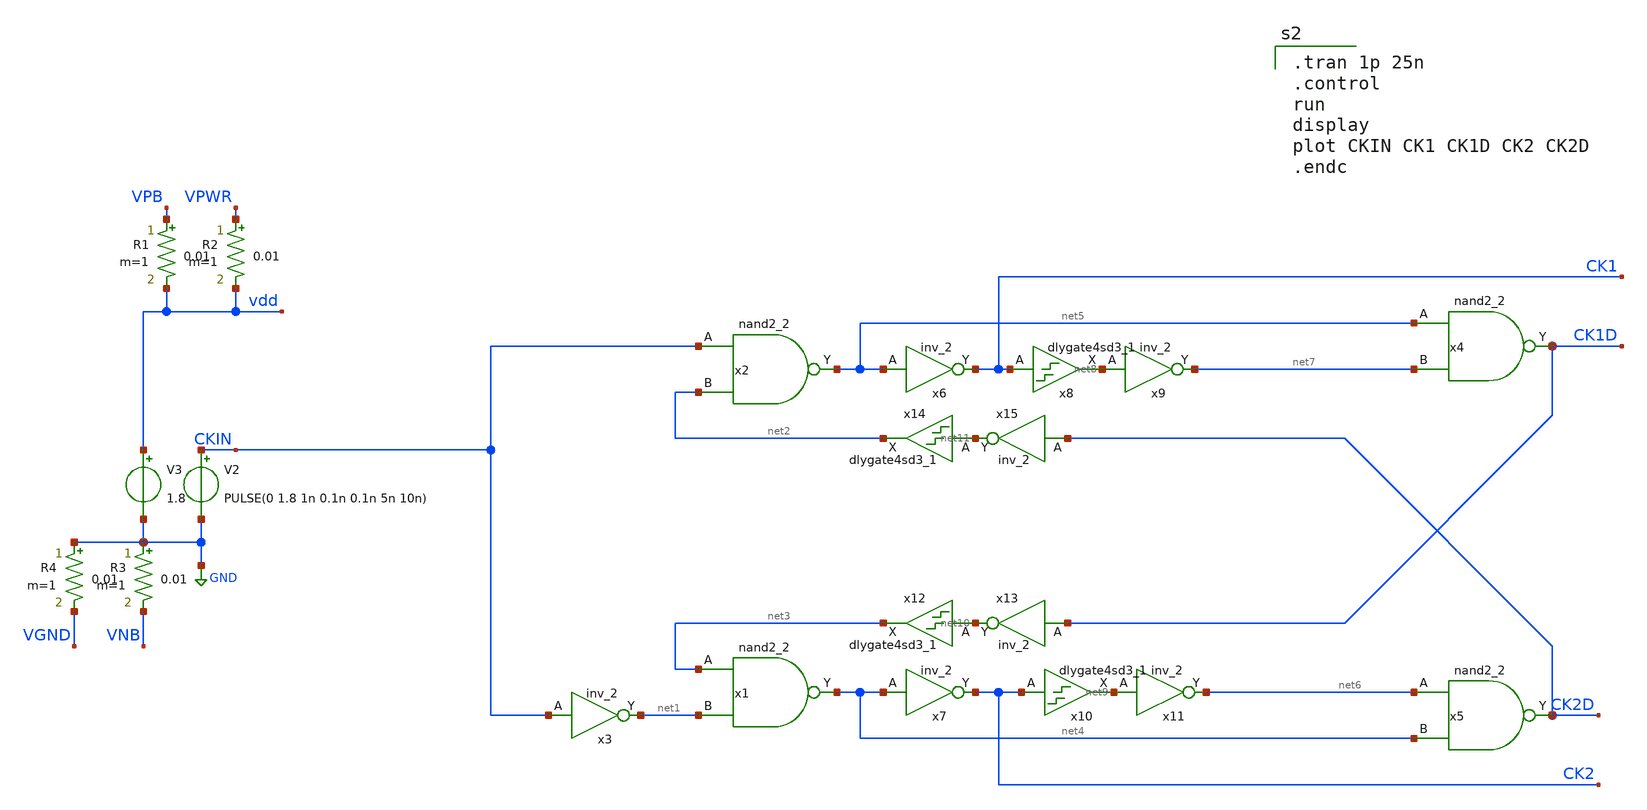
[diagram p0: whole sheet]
** sch_path: xschem/adc_non_overlap.sch
**.subckt adc_non_overlap
V2 CKIN GND PULSE(0 1.8 1n 0.1n 0.1n 5n 10n)
V3 vdd GND 1.8
x2 CKIN net2 VGND VNB VPB VPWR net5 sky130_fd_sc_hd__nand2_2
x1 net3 net1 VGND VNB VPB VPWR net4 sky130_fd_sc_hd__nand2_2
x3 CKIN VGND VNB VPB VPWR net1 sky130_fd_sc_hd__inv_2
x4 net5 net7 VGND VNB VPB VPWR CK1D sky130_fd_sc_hd__nand2_2
x5 net6 net4 VGND VNB VPB VPWR CK2D sky130_fd_sc_hd__nand2_2
x6 net5 VGND VNB VPB VPWR CK1 sky130_fd_sc_hd__inv_2
x7 net4 VGND VNB VPB VPWR CK2 sky130_fd_sc_hd__inv_2
x8 CK1 VGND VNB VPB VPWR net8 sky130_fd_sc_hd__dlygate4sd3_1
x9 net8 VGND VNB VPB VPWR net7 sky130_fd_sc_hd__inv_2
x10 CK2 VGND VNB VPB VPWR net9 sky130_fd_sc_hd__dlygate4sd3_1
x11 net9 VGND VNB VPB VPWR net6 sky130_fd_sc_hd__inv_2
x12 net10 VGND VNB VPB VPWR net3 sky130_fd_sc_hd__dlygate4sd3_1
x13 CK1D VGND VNB VPB VPWR net10 sky130_fd_sc_hd__inv_2
x14 net11 VGND VNB VPB VPWR net2 sky130_fd_sc_hd__dlygate4sd3_1
x15 CK2D VGND VNB VPB VPWR net11 sky130_fd_sc_hd__inv_2
R1 VPB vdd 0.01 m=1
R2 VPWR vdd 0.01 m=1
R3 GND VNB 0.01 m=1
R4 GND VGND 0.01 m=1
**** begin user architecture code
.lib $::SKYWATER_MODELS/sky130.lib.spice tt
.include /home/al/openmpw/pdk_1/sky130B/libs.ref/sky130_fd_sc_hd/spice/sky130_fd_sc_hd.spice


.tran 1p 25n
.control
run
display
plot CKIN CK1 CK1D CK2 CK2D
.endc


**** end user architecture code
**.ends
.GLOBAL GND
.end
